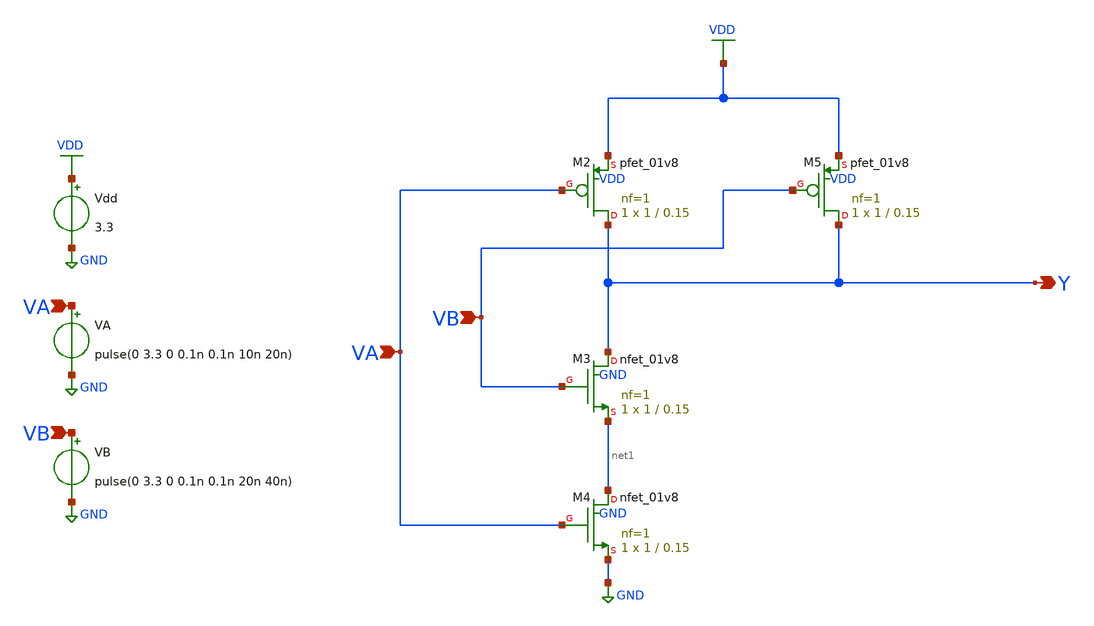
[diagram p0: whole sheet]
** sch_path: nand/nand_skywater_fets.sch
**.subckt nand_skywater_fets Y VA VA VB VB
*.opin Y
*.ipin VA
*.ipin VA
*.ipin VB
*.ipin VB
Vdd VDD GND 3.3
.save i(vdd)
VA VA GND pulse(0 3.3 0 0.1n 0.1n 10n 20n)
VB VB GND pulse(0 3.3 0 0.1n 0.1n 20n 40n)
XM4 net1 VA GND GND sky130_fd_pr__nfet_01v8 L=0.15 W=1 nf=1 ad='int((1 + 1)/2) * 1 / 1 * 0.29' as='int((1 + 2)/2) * 1 / 1 * 0.29'
+ pd='2*int((1 + 1)/2) * (1 / 1 + 0.29)' ps='2*int((1 + 2)/2) * (1 / 1 + 0.29)' nrd='0.29 / 1 ' nrs='0.29 / 1 '
+ sa=0 sb=0 sd=0 mult=1 m=1
XM3 Y VB net1 GND sky130_fd_pr__nfet_01v8 L=0.15 W=1 nf=1 ad='int((1 + 1)/2) * 1 / 1 * 0.29' as='int((1 + 2)/2) * 1 / 1 * 0.29'
+ pd='2*int((1 + 1)/2) * (1 / 1 + 0.29)' ps='2*int((1 + 2)/2) * (1 / 1 + 0.29)' nrd='0.29 / 1 ' nrs='0.29 / 1 '
+ sa=0 sb=0 sd=0 mult=1 m=1
XM2 Y VA VDD VDD sky130_fd_pr__pfet_01v8 L=0.15 W=1 nf=1 ad='int((1 + 1)/2) * 1 / 1 * 0.29' as='int((1 + 2)/2) * 1 / 1 * 0.29'
+ pd='2*int((1 + 1)/2) * (1 / 1 + 0.29)' ps='2*int((1 + 2)/2) * (1 / 1 + 0.29)' nrd='0.29 / 1 ' nrs='0.29 / 1 '
+ sa=0 sb=0 sd=0 mult=1 m=1
XM5 Y VB VDD VDD sky130_fd_pr__pfet_01v8 L=0.15 W=1 nf=1 ad='int((1 + 1)/2) * 1 / 1 * 0.29' as='int((1 + 2)/2) * 1 / 1 * 0.29'
+ pd='2*int((1 + 1)/2) * (1 / 1 + 0.29)' ps='2*int((1 + 2)/2) * (1 / 1 + 0.29)' nrd='0.29 / 1 ' nrs='0.29 / 1 '
+ sa=0 sb=0 sd=0 mult=1 m=1
**** begin user architecture code

.lib /usr/local/share/pdk/sky130B/libs.tech/ngspice/sky130.lib.spice tt
.option wnflag=1

**** end user architecture code
**.ends
.GLOBAL VDD
.GLOBAL GND
**** begin user architecture code


.save v(va) v(vb) v(y)
.tran 0.1n 200n


**** end user architecture code
.end
